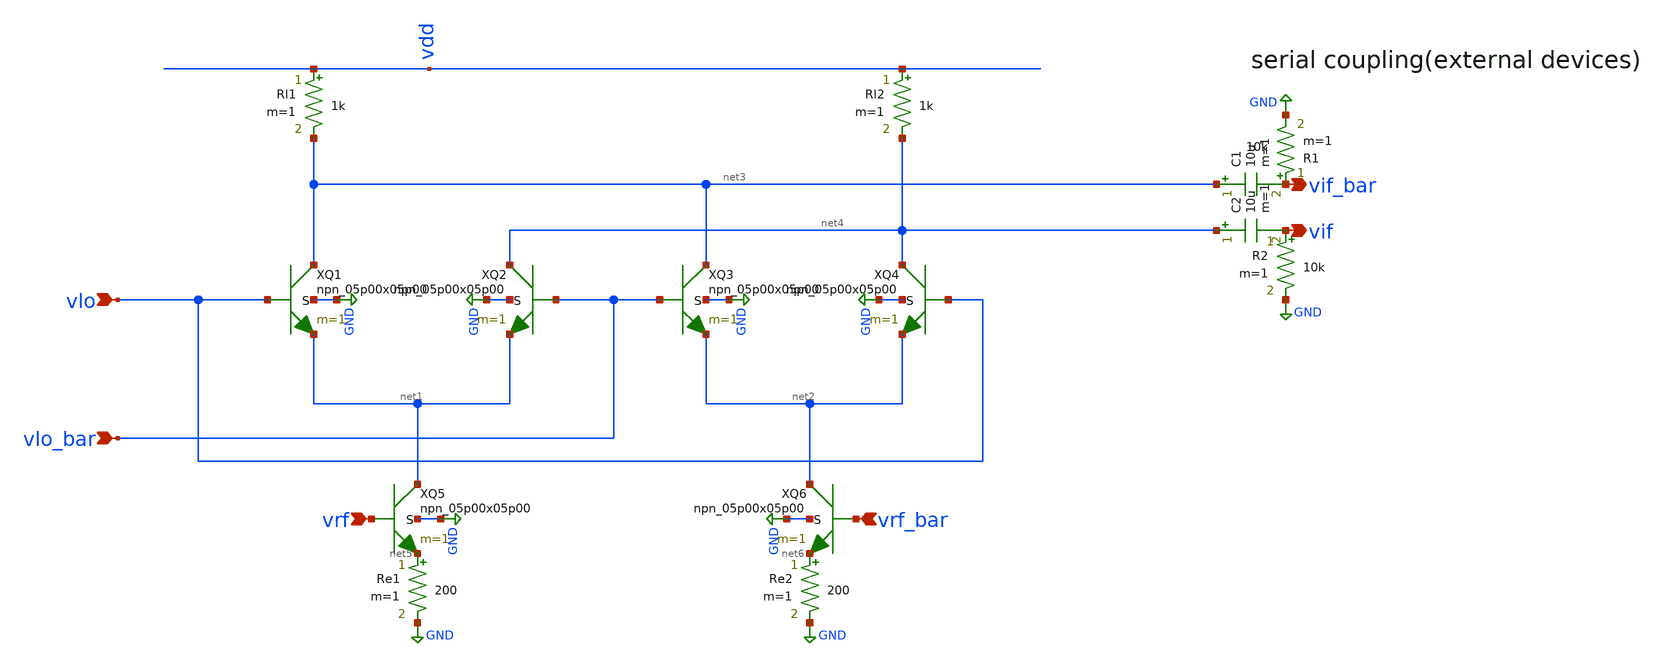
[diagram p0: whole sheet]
** sch_path: verified/0002_gc_tb.sch
**.subckt 0002_gc_tb vrf vlo vlo_bar vif_bar vif vrf_bar
*.ipin vrf
*.ipin vlo
*.ipin vlo_bar
*.opin vif_bar
*.opin vif
*.ipin vrf_bar
XQ1 net3 vlo net1 GND npn_05p00x05p00 m=1
XQ2 net4 vlo_bar net1 GND npn_05p00x05p00 m=1
XQ3 net3 vlo_bar net2 GND npn_05p00x05p00 m=1
XQ4 net4 vlo net2 GND npn_05p00x05p00 m=1
XQ5 net1 vrf net5 GND npn_05p00x05p00 m=1
XQ6 net2 vrf_bar net6 GND npn_05p00x05p00 m=1
Re1 net5 GND 200 m=1
Re2 net6 GND 200 m=1
Rl1 vdd net3 1k m=1
Rl2 vdd net4 1k m=1
C1 net3 vif_bar 10u m=1
C2 net4 vif 10u m=1
R1 vif_bar GND 10k m=1
R2 vif GND 10k m=1
**** begin user architecture code




.include '/home/user/.volare/volare/sky130/versions/0fe599b2afb6708d281543108caf8310912f54af/volare/gf180mcu/versions/0fe599b2afb6708d281543108caf8310912f54af/gf180mcuD/libs.tech/ngspice/design.ngspice'
.lib '/home/user/.volare/volare/sky130/versions/0fe599b2afb6708d281543108caf8310912f54af/volare/gf180mcu/versions/0fe599b2afb6708d281543108caf8310912f54af/gf180mcuD/libs.tech/ngspice/sm141064.ngspice' bjt_typical

.param VCC=3.3
VDD vdd GND 3.3



Vrf  vrf     GND sin(1.5 0.05 1k)
Vrfb vrf_bar GND sin(1.5 -0.05 1k)


Vlo  vlo     GND sin(1.5 0.05 5k)
Vlob vlo_bar GND sin(1.5 -0.05 5k)

.tran 1u 5m
.save all
.control
run
plot v(vif) v(vif_bar)
plot v(vif) - v(vif_bar)
linearize
fft v(vif) v(vif_bar)
plot mag(v(vif)) xlimit 0 10k

.endc




**** end user architecture code
**.ends
.GLOBAL GND
.end
